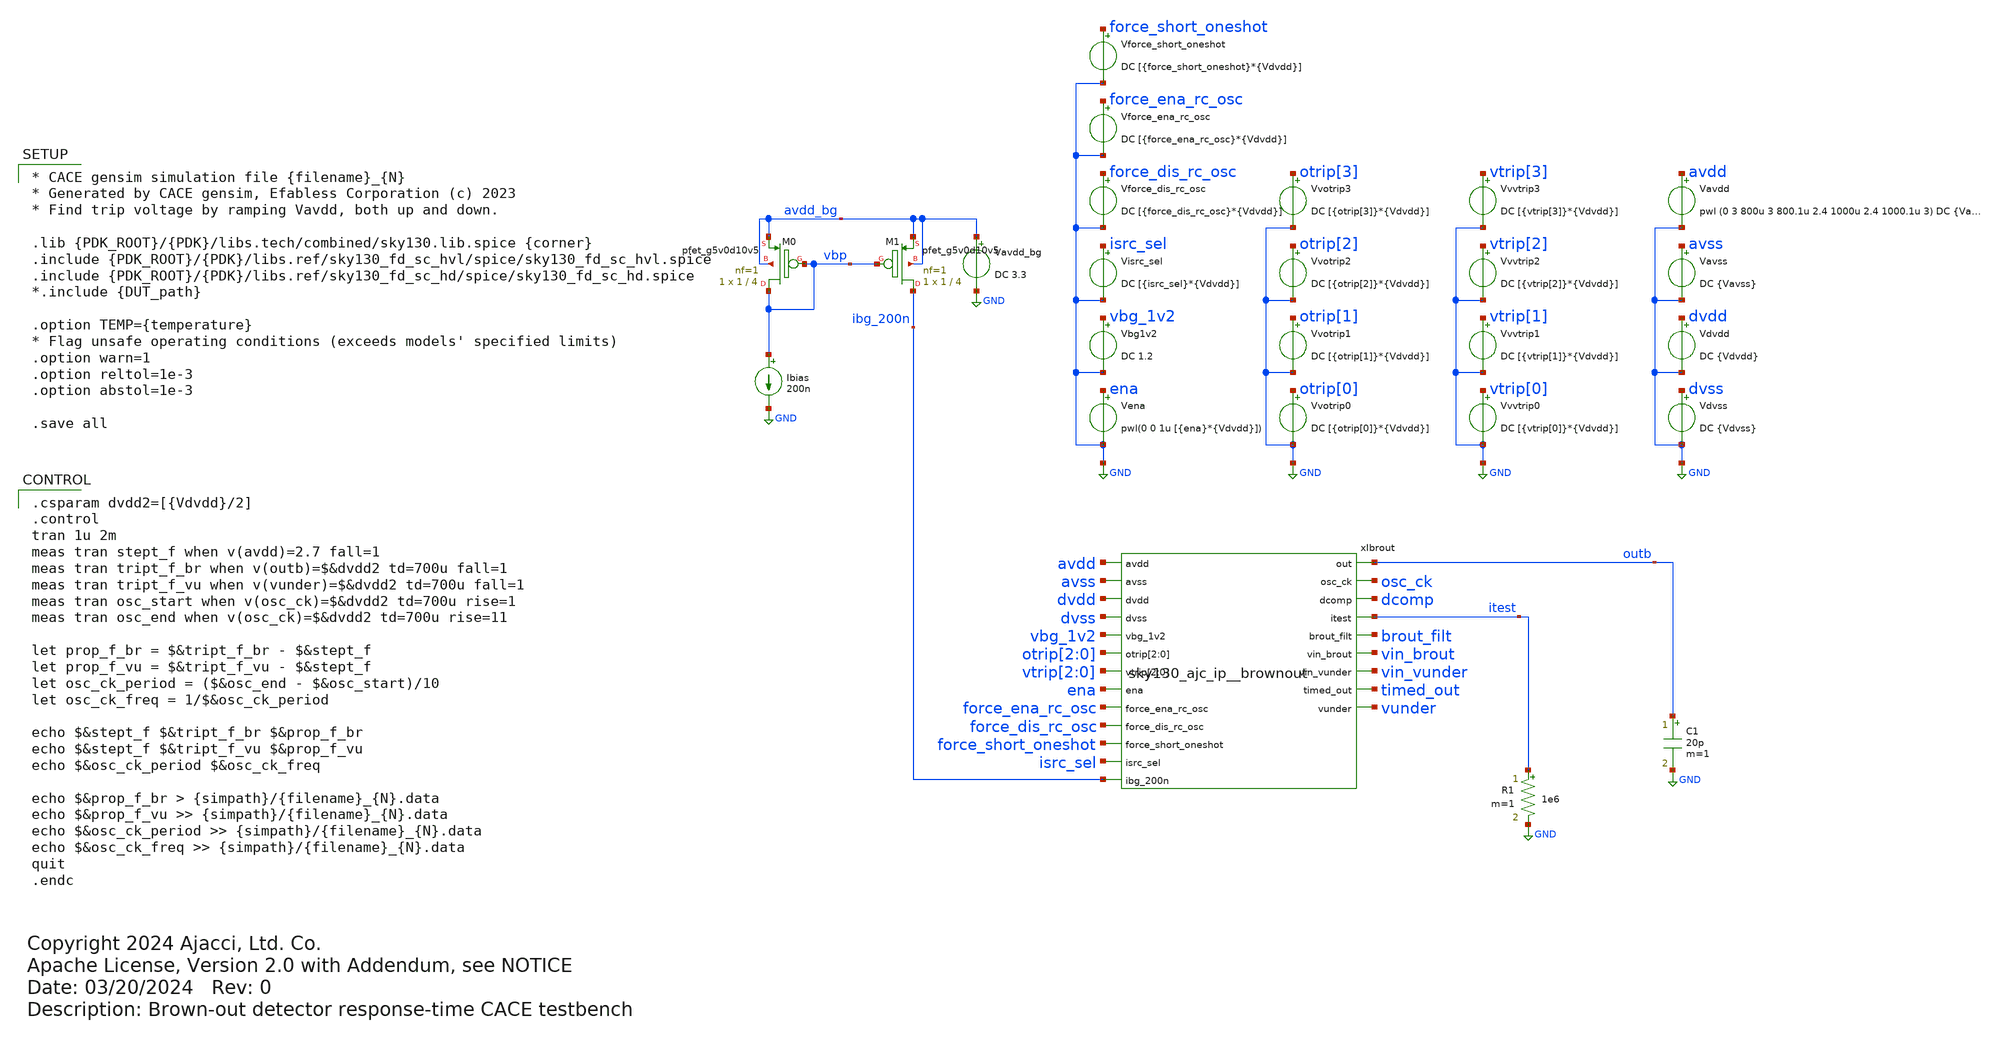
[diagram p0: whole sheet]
** sch_path: cace/response_time.sch
* Copyright 2024 Ajacci, Ltd. Co.
* Apache License, Version 2.0 with Addendum, see NOTICE
**.subckt response_time
Ibias vbp GND 200n
XM1 ibg_200n vbp avdd_bg avdd_bg sky130_fd_pr__pfet_g5v0d10v5 L=4 W=1 nf=1 ad='int((nf+1)/2) * W/nf * 0.29'
+ as='int((nf+2)/2) * W/nf * 0.29' pd='2*int((nf+1)/2) * (W/nf + 0.29)' ps='2*int((nf+2)/2) * (W/nf + 0.29)'
+ nrd='0.29 / W' nrs='0.29 / W' sa=0 sb=0 sd=0 mult=1 m=1
XM0 vbp vbp avdd_bg avdd_bg sky130_fd_pr__pfet_g5v0d10v5 L=4 W=1 nf=1 ad='int((nf+1)/2) * W/nf * 0.29'
+ as='int((nf+2)/2) * W/nf * 0.29' pd='2*int((nf+1)/2) * (W/nf + 0.29)' ps='2*int((nf+2)/2) * (W/nf + 0.29)'
+ nrd='0.29 / W' nrs='0.29 / W' sa=0 sb=0 sd=0 mult=1 m=1
R1 itest GND 1e6 m=1
C1 outb GND 20p m=1
xIbrout avdd avss outb dvdd osc_ck dvss dcomp vbg_1v2 otrip[2] otrip[1] otrip[0] itest brout_filt
+ vtrip[2] vtrip[1] vtrip[0] vin_brout ena force_ena_rc_osc vin_vunder force_dis_rc_osc timed_out vunder
+ force_short_oneshot isrc_sel ibg_200n sky130_ajc_ip__brownout
Vavss avss GND DC {Vavss}
Vena ena GND pwl(0 0 1u [{ena}*{Vdvdd}])
Vavdd avdd GND pwl (0 3 800u 3 800.1u 2.4 1000u 2.4 1000.1u 3) DC {Vavdd}
.save i(vavdd)
Vbg1v2 vbg_1v2 GND DC 1.2
Vdvss dvss GND DC {Vdvss}
Vdvdd dvdd GND DC {Vdvdd}
.save i(vdvdd)
Vvotrip0 otrip[0] GND DC [{otrip[0]}*{Vdvdd}]
.save i(vvotrip0)
Vvotrip1 otrip[1] GND DC [{otrip[1]}*{Vdvdd}]
.save i(vvotrip1)
Vvotrip2 otrip[2] GND DC [{otrip[2]}*{Vdvdd}]
.save i(vvotrip2)
Vvotrip3 otrip[3] GND DC [{otrip[3]}*{Vdvdd}]
.save i(vvotrip3)
Visrc_sel isrc_sel GND DC [{isrc_sel}*{Vdvdd}]
Vvvtrip0 vtrip[0] GND DC [{vtrip[0]}*{Vdvdd}]
.save i(vvvtrip0)
Vvvtrip1 vtrip[1] GND DC [{vtrip[1]}*{Vdvdd}]
.save i(vvvtrip1)
Vvvtrip2 vtrip[2] GND DC [{vtrip[2]}*{Vdvdd}]
.save i(vvvtrip2)
Vvvtrip3 vtrip[3] GND DC [{vtrip[3]}*{Vdvdd}]
.save i(vvvtrip3)
Vavdd_bg avdd_bg GND DC 3.3
Vforce_dis_rc_osc force_dis_rc_osc GND DC [{force_dis_rc_osc}*{Vdvdd}]
Vforce_short_oneshot force_short_oneshot GND DC [{force_short_oneshot}*{Vdvdd}]
Vforce_ena_rc_osc force_ena_rc_osc GND DC [{force_ena_rc_osc}*{Vdvdd}]
**** begin user architecture code

* CACE gensim simulation file {filename}_{N}
* Generated by CACE gensim, Efabless Corporation (c) 2023
* Find trip voltage by ramping Vavdd, both up and down.

.lib {PDK_ROOT}/{PDK}/libs.tech/combined/sky130.lib.spice {corner}
.include {PDK_ROOT}/{PDK}/libs.ref/sky130_fd_sc_hvl/spice/sky130_fd_sc_hvl.spice
.include {PDK_ROOT}/{PDK}/libs.ref/sky130_fd_sc_hd/spice/sky130_fd_sc_hd.spice
*.include {DUT_path}

.option TEMP={temperature}
* Flag unsafe operating conditions (exceeds models' specified limits)
.option warn=1
.option reltol=1e-3
.option abstol=1e-3

.save all



.csparam dvdd2=[{Vdvdd}/2]
.control
tran 1u 2m
meas tran stept_f when v(avdd)=2.7 fall=1
meas tran tript_f_br when v(outb)=$&dvdd2 td=700u fall=1
meas tran tript_f_vu when v(vunder)=$&dvdd2 td=700u fall=1
meas tran osc_start when v(osc_ck)=$&dvdd2 td=700u rise=1
meas tran osc_end when v(osc_ck)=$&dvdd2 td=700u rise=11

let prop_f_br = $&tript_f_br - $&stept_f
let prop_f_vu = $&tript_f_vu - $&stept_f
let osc_ck_period = ($&osc_end - $&osc_start)/10
let osc_ck_freq = 1/$&osc_ck_period

echo $&stept_f $&tript_f_br $&prop_f_br
echo $&stept_f $&tript_f_vu $&prop_f_vu
echo $&osc_ck_period $&osc_ck_freq

echo $&prop_f_br > {simpath}/{filename}_{N}.data
echo $&prop_f_vu >> {simpath}/{filename}_{N}.data
echo $&osc_ck_period >> {simpath}/{filename}_{N}.data
echo $&osc_ck_freq >> {simpath}/{filename}_{N}.data
quit
.endc


**** end user architecture code
**.ends
.GLOBAL GND
.end
